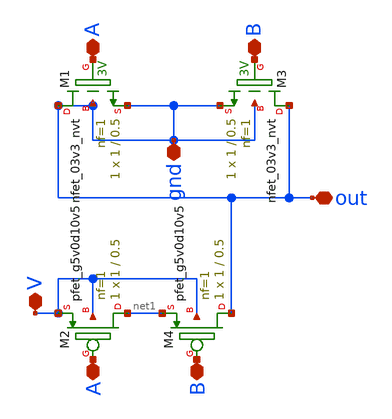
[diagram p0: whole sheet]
** sch_path: SAR_ADC/xschem/designs/nandgate.sch
**.subckt nandgate A out A gnd V B B
*.iopin A
*.iopin out
*.iopin A
*.iopin gnd
*.iopin V
*.iopin B
*.iopin B
XM1 out A out out sky130_fd_pr__nfet_03v3_nvt L=0.5 W=1 nf=1 ad='int((nf+1)/2) * W/nf * 0.29' as='int((nf+2)/2) * W/nf * 0.29'
+ pd='2*int((nf+1)/2) * (W/nf + 0.29)' ps='2*int((nf+2)/2) * (W/nf + 0.29)' nrd='0.29 / W' nrs='0.29 / W'
+ sa=0 sb=0 sd=0 mult=1 m=1
XM2 net1 A V V sky130_fd_pr__pfet_g5v0d10v5 L=0.5 W=1 nf=1 ad='int((nf+1)/2) * W/nf * 0.29' as='int((nf+2)/2) * W/nf * 0.29'
+ pd='2*int((nf+1)/2) * (W/nf + 0.29)' ps='2*int((nf+2)/2) * (W/nf + 0.29)' nrd='0.29 / W' nrs='0.29 / W'
+ sa=0 sb=0 sd=0 mult=1 m=1
XM3 out B out out sky130_fd_pr__nfet_03v3_nvt L=0.5 W=1 nf=1 ad='int((nf+1)/2) * W/nf * 0.29' as='int((nf+2)/2) * W/nf * 0.29'
+ pd='2*int((nf+1)/2) * (W/nf + 0.29)' ps='2*int((nf+2)/2) * (W/nf + 0.29)' nrd='0.29 / W' nrs='0.29 / W'
+ sa=0 sb=0 sd=0 mult=1 m=1
XM4 out B net1 V sky130_fd_pr__pfet_g5v0d10v5 L=0.5 W=1 nf=1 ad='int((nf+1)/2) * W/nf * 0.29' as='int((nf+2)/2) * W/nf * 0.29'
+ pd='2*int((nf+1)/2) * (W/nf + 0.29)' ps='2*int((nf+2)/2) * (W/nf + 0.29)' nrd='0.29 / W' nrs='0.29 / W'
+ sa=0 sb=0 sd=0 mult=1 m=1
**.ends
.end
